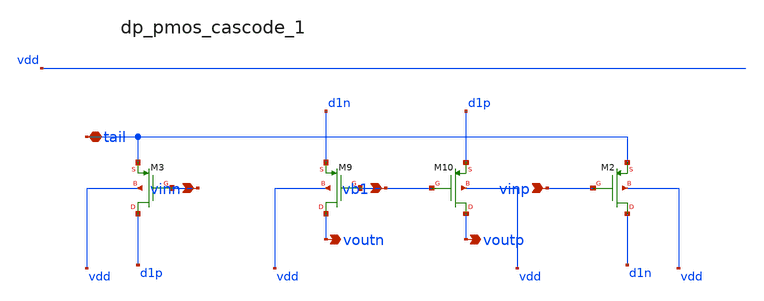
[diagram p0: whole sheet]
** sch_path: analog-db/raw/amp_027_fan_rrl_ota/hier/blocks/dp_pmos_cascode_1.sch
**.subckt dp_pmos_cascode_1 vinn vb1 vinp tail voutn voutp
*.ipin vinn
*.ipin vb1
*.ipin vinp
*.iopin tail
*.opin voutn
*.opin voutp
XM10 voutp vb1 d1p vdd sg13_lv_pmos w=x_dut_xm10_w l=x_dut_xm10_l ng=1 m=x_dut_xm10_m
XM2 d1n vinp tail vdd sg13_lv_pmos w=x_dut_xm2_w l=x_dut_xm2_l ng=1 m=x_dut_xm2_m
XM3 d1p vinn tail vdd sg13_lv_pmos w=x_dut_xm3_w l=x_dut_xm3_l ng=1 m=x_dut_xm3_m
XM9 voutn vb1 d1n vdd sg13_lv_pmos w=x_dut_xm9_w l=x_dut_xm9_l ng=1 m=x_dut_xm9_m
**.ends
.end
